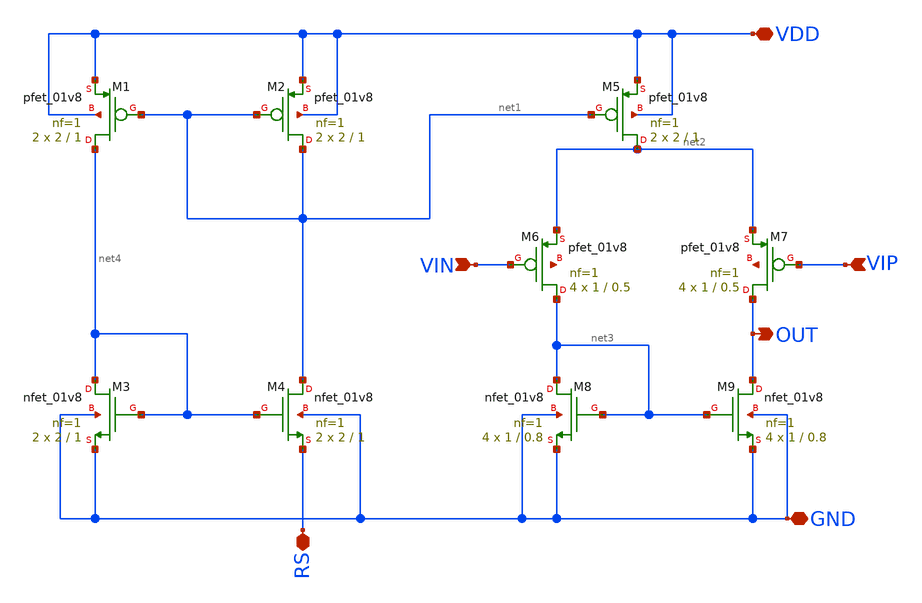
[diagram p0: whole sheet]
** sch_path: opamp/xschem/opamp.sch
**.subckt opamp VDD GND RS VIN VIP OUT
*.iopin VDD
*.iopin GND
*.iopin RS
*.ipin VIN
*.ipin VIP
*.opin OUT
XM2 net1 net1 VDD VDD sky130_fd_pr__pfet_01v8 L=1 W=2 nf=1 ad='int((nf+1)/2) * W/nf * 0.29' as='int((nf+2)/2) * W/nf * 0.29'
+ pd='2*int((nf+1)/2) * (W/nf + 0.29)' ps='2*int((nf+2)/2) * (W/nf + 0.29)' nrd='0.29 / W' nrs='0.29 / W'
+ sa=0 sb=0 sd=0 mult=2 m=2
XM1 net4 net1 VDD VDD sky130_fd_pr__pfet_01v8 L=1 W=2 nf=1 ad='int((nf+1)/2) * W/nf * 0.29' as='int((nf+2)/2) * W/nf * 0.29'
+ pd='2*int((nf+1)/2) * (W/nf + 0.29)' ps='2*int((nf+2)/2) * (W/nf + 0.29)' nrd='0.29 / W' nrs='0.29 / W'
+ sa=0 sb=0 sd=0 mult=2 m=2
XM5 net2 net1 VDD VDD sky130_fd_pr__pfet_01v8 L=1 W=2 nf=1 ad='int((nf+1)/2) * W/nf * 0.29' as='int((nf+2)/2) * W/nf * 0.29'
+ pd='2*int((nf+1)/2) * (W/nf + 0.29)' ps='2*int((nf+2)/2) * (W/nf + 0.29)' nrd='0.29 / W' nrs='0.29 / W'
+ sa=0 sb=0 sd=0 mult=2 m=2
XM6 net3 VIN net2 net5 sky130_fd_pr__pfet_01v8 L=0.5 W=1 nf=1 ad='int((nf+1)/2) * W/nf * 0.29' as='int((nf+2)/2) * W/nf * 0.29'
+ pd='2*int((nf+1)/2) * (W/nf + 0.29)' ps='2*int((nf+2)/2) * (W/nf + 0.29)' nrd='0.29 / W' nrs='0.29 / W'
+ sa=0 sb=0 sd=0 mult=4 m=4
XM7 OUT VIP net2 net6 sky130_fd_pr__pfet_01v8 L=0.5 W=1 nf=1 ad='int((nf+1)/2) * W/nf * 0.29' as='int((nf+2)/2) * W/nf * 0.29'
+ pd='2*int((nf+1)/2) * (W/nf + 0.29)' ps='2*int((nf+2)/2) * (W/nf + 0.29)' nrd='0.29 / W' nrs='0.29 / W'
+ sa=0 sb=0 sd=0 mult=4 m=4
XM4 net1 net4 RS GND sky130_fd_pr__nfet_01v8 L=1 W=2 nf=1 ad='int((nf+1)/2) * W/nf * 0.29' as='int((nf+2)/2) * W/nf * 0.29'
+ pd='2*int((nf+1)/2) * (W/nf + 0.29)' ps='2*int((nf+2)/2) * (W/nf + 0.29)' nrd='0.29 / W' nrs='0.29 / W'
+ sa=0 sb=0 sd=0 mult=2 m=2
XM9 OUT net3 GND GND sky130_fd_pr__nfet_01v8 L=0.8 W=1 nf=1 ad='int((nf+1)/2) * W/nf * 0.29' as='int((nf+2)/2) * W/nf * 0.29'
+ pd='2*int((nf+1)/2) * (W/nf + 0.29)' ps='2*int((nf+2)/2) * (W/nf + 0.29)' nrd='0.29 / W' nrs='0.29 / W'
+ sa=0 sb=0 sd=0 mult=4 m=4
XM8 net3 net3 GND GND sky130_fd_pr__nfet_01v8 L=0.8 W=1 nf=1 ad='int((nf+1)/2) * W/nf * 0.29' as='int((nf+2)/2) * W/nf * 0.29'
+ pd='2*int((nf+1)/2) * (W/nf + 0.29)' ps='2*int((nf+2)/2) * (W/nf + 0.29)' nrd='0.29 / W' nrs='0.29 / W'
+ sa=0 sb=0 sd=0 mult=4 m=4
XM3 net4 net4 GND GND sky130_fd_pr__nfet_01v8 L=1 W=2 nf=1 ad='int((nf+1)/2) * W/nf * 0.29' as='int((nf+2)/2) * W/nf * 0.29'
+ pd='2*int((nf+1)/2) * (W/nf + 0.29)' ps='2*int((nf+2)/2) * (W/nf + 0.29)' nrd='0.29 / W' nrs='0.29 / W'
+ sa=0 sb=0 sd=0 mult=2 m=2
**.ends
.end
